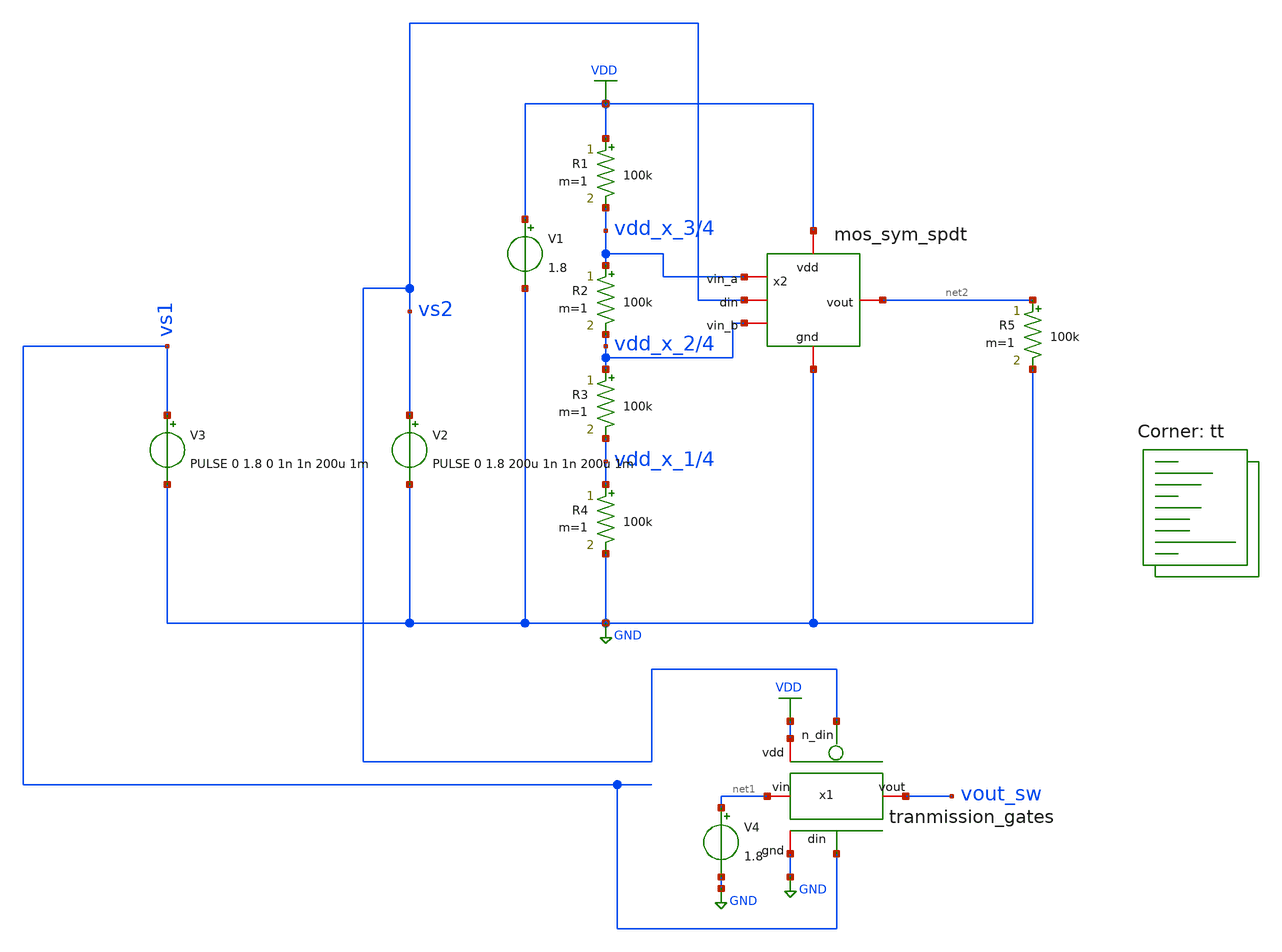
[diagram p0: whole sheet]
** sch_path: Schematics/adc.sch
**.subckt adc
V1 VDD GND 1.8
R1 VDD vdd_x_3/4 100k m=1
R2 vdd_x_3/4 vdd_x_2/4 100k m=1
R3 vdd_x_2/4 vdd_x_1/4 100k m=1
R4 vdd_x_1/4 GND 100k m=1
V2 vs2 GND PULSE 0 1.8 200u 1n 1n 200u 1m
V3 vs1 GND PULSE 0 1.8 0 1n 1n 200u 1m
V4 net1 GND 1.8
x1 vs2 VDD vout_sw net1 GND vs1 tranmission_gates
x2 VDD vdd_x_3/4 net2 vs2 vdd_x_2/4 GND mos_sym_spdt
R5 net2 GND 100k m=1
**** begin user architecture code
.lib $::SKYWATER_MODELS/sky130.lib.spice tt
**** end user architecture code
**.ends

* expanding   symbol:  Symbols/tranmission_gates.sym # of pins=6
** sym_path: Symbols/tranmission_gates.sym
** sch_path: Symbols/tranmission_gates.sch
.subckt tranmission_gates n_din vdd vout vin gnd din
*.ipin din
*.ipin n_din
*.iopin vdd
*.iopin gnd
*.iopin vin
*.iopin vout
XM3 vout n_din vin vdd sky130_fd_pr__pfet_01v8 L=1 W=10 nf=1 ad='int((nf+1)/2) * W/nf * 0.29' as='int((nf+2)/2) * W/nf * 0.29'
+ pd='2*int((nf+1)/2) * (W/nf + 0.29)' ps='2*int((nf+2)/2) * (W/nf + 0.29)' nrd='0.29 / W' nrs='0.29 / W'
+ sa=0 sb=0 sd=0 mult=1 m=1
XM4 vin din vout gnd sky130_fd_pr__nfet_01v8 L=1 W=1 nf=1 ad='int((1 + 1)/2) * 1 / 1 * 0.29' as='int((1 + 2)/2) * 1 / 1 * 0.29'
+ pd='2*int((1 + 1)/2) * (1 / 1 + 0.29)' ps='2*int((1 + 2)/2) * (1 / 1 + 0.29)' nrd='0.29 / 1 ' nrs='0.29 / 1 '
+ sa=0 sb=0 sd=0 mult=1 m=1
.ends


* expanding   symbol:  Symbols/mos_sym_spdt.sym # of pins=6
** sym_path: Symbols/mos_sym_spdt.sym
** sch_path: Symbols/mos_sym_spdt.sch
.subckt mos_sym_spdt vdd vin_a vout din vin_b gnd
*.iopin vout
*.iopin vin_a
*.iopin vin_b
*.iopin vdd
*.iopin gnd
*.ipin din
XM3 n_din din vdd vdd sky130_fd_pr__pfet_01v8 L=1 W=1 nf=1 ad='int((nf+1)/2) * W/nf * 0.29' as='int((nf+2)/2) * W/nf * 0.29'
+ pd='2*int((nf+1)/2) * (W/nf + 0.29)' ps='2*int((nf+2)/2) * (W/nf + 0.29)' nrd='0.29 / W' nrs='0.29 / W'
+ sa=0 sb=0 sd=0 mult=1 m=1
XM4 n_din din net1 net1 sky130_fd_pr__nfet_01v8 L=1 W=1 nf=1 ad='int((1 + 1)/2) * 1 / 1 * 0.29' as='int((1 + 2)/2) * 1 / 1 * 0.29'
+ pd='2*int((1 + 1)/2) * (1 / 1 + 0.29)' ps='2*int((1 + 2)/2) * (1 / 1 + 0.29)' nrd='0.29 / 1 ' nrs='0.29 / 1 '
+ sa=0 sb=0 sd=0 mult=1 m=1
XM1 net2 n_din vdd vdd sky130_fd_pr__pfet_01v8 L=1 W=1 nf=1 ad='int((nf+1)/2) * W/nf * 0.29' as='int((nf+2)/2) * W/nf * 0.29'
+ pd='2*int((nf+1)/2) * (W/nf + 0.29)' ps='2*int((nf+2)/2) * (W/nf + 0.29)' nrd='0.29 / W' nrs='0.29 / W'
+ sa=0 sb=0 sd=0 mult=1 m=1
XM2 net2 n_din gnd gnd sky130_fd_pr__nfet_01v8 L=1 W=1 nf=1 ad='int((1 + 1)/2) * 1 / 1 * 0.29' as='int((1 + 2)/2) * 1 / 1 * 0.29'
+ pd='2*int((1 + 1)/2) * (1 / 1 + 0.29)' ps='2*int((1 + 2)/2) * (1 / 1 + 0.29)' nrd='0.29 / 1 ' nrs='0.29 / 1 '
+ sa=0 sb=0 sd=0 mult=1 m=1
XM5 vout n_din vin_a vdd sky130_fd_pr__pfet_01v8 L=1 W=10 nf=1 ad='int((nf+1)/2) * W/nf * 0.29' as='int((nf+2)/2) * W/nf * 0.29'
+ pd='2*int((nf+1)/2) * (W/nf + 0.29)' ps='2*int((nf+2)/2) * (W/nf + 0.29)' nrd='0.29 / W' nrs='0.29 / W'
+ sa=0 sb=0 sd=0 mult=1 m=1
XM6 vin_a net2 vout gnd sky130_fd_pr__nfet_01v8 L=1 W=1 nf=1 ad='int((1 + 1)/2) * 1 / 1 * 0.29' as='int((1 + 2)/2) * 1 / 1 * 0.29'
+ pd='2*int((1 + 1)/2) * (1 / 1 + 0.29)' ps='2*int((1 + 2)/2) * (1 / 1 + 0.29)' nrd='0.29 / 1 ' nrs='0.29 / 1 '
+ sa=0 sb=0 sd=0 mult=1 m=1
XM7 vout net2 vin_b vdd sky130_fd_pr__pfet_01v8 L=1 W=10 nf=1 ad='int((nf+1)/2) * W/nf * 0.29' as='int((nf+2)/2) * W/nf * 0.29'
+ pd='2*int((nf+1)/2) * (W/nf + 0.29)' ps='2*int((nf+2)/2) * (W/nf + 0.29)' nrd='0.29 / W' nrs='0.29 / W'
+ sa=0 sb=0 sd=0 mult=1 m=1
XM8 vin_b n_din vout gnd sky130_fd_pr__nfet_01v8 L=1 W=1 nf=1 ad='int((1 + 1)/2) * 1 / 1 * 0.29' as='int((1 + 2)/2) * 1 / 1 * 0.29'
+ pd='2*int((1 + 1)/2) * (1 / 1 + 0.29)' ps='2*int((1 + 2)/2) * (1 / 1 + 0.29)' nrd='0.29 / 1 ' nrs='0.29 / 1 '
+ sa=0 sb=0 sd=0 mult=1 m=1
.ends

.GLOBAL GND
.GLOBAL VDD
**** begin user architecture code

.options savecurrents
.tran 0.1m 1m uic
.save all
.control
	run
	write adc.raw
*plot all.vout
.endc


**** end user architecture code
.end
